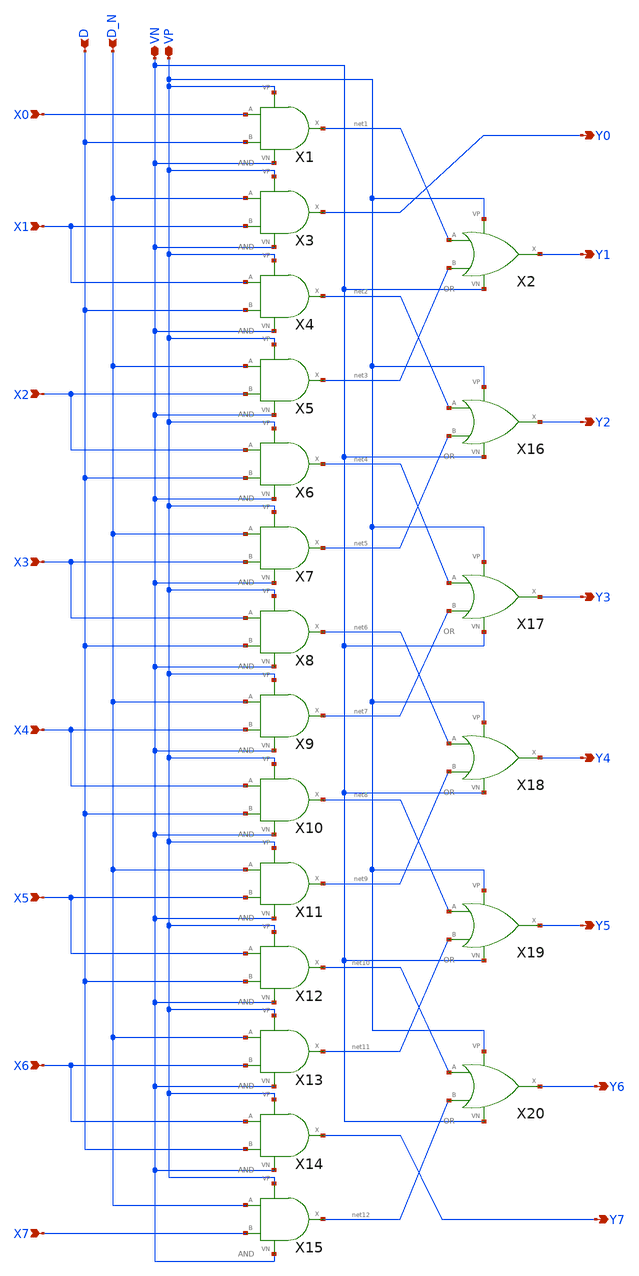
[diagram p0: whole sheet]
** sch_path: projekat_spice/layout/shifter/SHIFTER.sch
**.subckt SHIFTER VP VN X0 X1 X2 X3 X4 X5 X6 X7 D D_N Y0 Y1 Y2 Y3 Y4 Y5 Y6 Y7
*.iopin VP
*.iopin VN
*.ipin X0
*.ipin X1
*.ipin X2
*.ipin X3
*.ipin X4
*.ipin X5
*.ipin X6
*.ipin X7
*.ipin D
*.ipin D_N
*.opin Y0
*.opin Y1
*.opin Y2
*.opin Y3
*.opin Y4
*.opin Y5
*.opin Y6
*.opin Y7
X1 X0 D net1 VP VN AND
X3 D_N X1 Y0 VP VN AND
X4 X1 D net2 VP VN AND
X5 D_N X2 net3 VP VN AND
X6 X2 D net4 VP VN AND
X7 D_N X3 net5 VP VN AND
X8 X3 D net6 VP VN AND
X9 D_N X4 net7 VP VN AND
X10 X4 D net8 VP VN AND
X11 D_N X5 net9 VP VN AND
X12 X5 D net10 VP VN AND
X13 D_N X6 net11 VP VN AND
X14 X6 D Y7 VP VN AND
X15 D_N X7 net12 VP VN AND
X2 net1 net3 Y1 VP VN OR
X16 net2 net5 Y2 VP VN OR
X17 net4 net7 Y3 VP VN OR
X18 net6 net9 Y4 VP VN OR
X19 net8 net11 Y5 VP VN OR
X20 net10 net12 Y6 VP VN OR
**.ends

* expanding   symbol:  /home/mihailo/projekat_sky130/projekat_layout/and/AND.sym # of pins=5
** sym_path: projekat_spice/layout/and/AND.sym
** sch_path: projekat_spice/layout/and/AND.sch
.subckt AND A B X VP VN
*.ipin A
*.ipin B
*.iopin VN
*.iopin VP
*.opin X
XM1 net1 A net2 VN sky130_fd_pr__nfet_01v8 L=0.15 W=1 nf=1 ad='int((nf+1)/2) * W/nf * 0.29' as='int((nf+2)/2) * W/nf * 0.29'
+ pd='2*int((nf+1)/2) * (W/nf + 0.29)' ps='2*int((nf+2)/2) * (W/nf + 0.29)' nrd='0.29 / W' nrs='0.29 / W'
+ sa=0 sb=0 sd=0 mult=1 m=1
XM2 net1 A VP VP sky130_fd_pr__pfet_01v8 L=0.15 W=1 nf=1 ad='int((nf+1)/2) * W/nf * 0.29' as='int((nf+2)/2) * W/nf * 0.29'
+ pd='2*int((nf+1)/2) * (W/nf + 0.29)' ps='2*int((nf+2)/2) * (W/nf + 0.29)' nrd='0.29 / W' nrs='0.29 / W'
+ sa=0 sb=0 sd=0 mult=1 m=1
XM3 net1 B VP VP sky130_fd_pr__pfet_01v8 L=0.15 W=1 nf=1 ad='int((nf+1)/2) * W/nf * 0.29' as='int((nf+2)/2) * W/nf * 0.29'
+ pd='2*int((nf+1)/2) * (W/nf + 0.29)' ps='2*int((nf+2)/2) * (W/nf + 0.29)' nrd='0.29 / W' nrs='0.29 / W'
+ sa=0 sb=0 sd=0 mult=1 m=1
XM4 net2 B VN VN sky130_fd_pr__nfet_01v8 L=0.15 W=1 nf=1 ad='int((nf+1)/2) * W/nf * 0.29' as='int((nf+2)/2) * W/nf * 0.29'
+ pd='2*int((nf+1)/2) * (W/nf + 0.29)' ps='2*int((nf+2)/2) * (W/nf + 0.29)' nrd='0.29 / W' nrs='0.29 / W'
+ sa=0 sb=0 sd=0 mult=1 m=1
XM5 X net1 VN VN sky130_fd_pr__nfet_01v8 L=0.15 W=1 nf=1 ad='int((nf+1)/2) * W/nf * 0.29' as='int((nf+2)/2) * W/nf * 0.29'
+ pd='2*int((nf+1)/2) * (W/nf + 0.29)' ps='2*int((nf+2)/2) * (W/nf + 0.29)' nrd='0.29 / W' nrs='0.29 / W'
+ sa=0 sb=0 sd=0 mult=1 m=1
XM6 X net1 VP VP sky130_fd_pr__pfet_01v8 L=0.15 W=1 nf=1 ad='int((nf+1)/2) * W/nf * 0.29' as='int((nf+2)/2) * W/nf * 0.29'
+ pd='2*int((nf+1)/2) * (W/nf + 0.29)' ps='2*int((nf+2)/2) * (W/nf + 0.29)' nrd='0.29 / W' nrs='0.29 / W'
+ sa=0 sb=0 sd=0 mult=1 m=1
.ends


* expanding   symbol:  /home/mihailo/projekat_sky130/projekat_layout/or/OR.sym # of pins=5
** sym_path: projekat_spice/layout/or/OR.sym
** sch_path: projekat_spice/layout/or/OR.sch
.subckt OR A B X VP VN
*.opin X
*.ipin A
*.ipin B
*.iopin VP
*.iopin VN
XM1 net2 A VN VN sky130_fd_pr__nfet_01v8 L=0.15 W=1 nf=1 ad='int((nf+1)/2) * W/nf * 0.29' as='int((nf+2)/2) * W/nf * 0.29'
+ pd='2*int((nf+1)/2) * (W/nf + 0.29)' ps='2*int((nf+2)/2) * (W/nf + 0.29)' nrd='0.29 / W' nrs='0.29 / W'
+ sa=0 sb=0 sd=0 mult=1 m=1
XM2 net1 A VP VP sky130_fd_pr__pfet_01v8 L=0.15 W=1 nf=1 ad='int((nf+1)/2) * W/nf * 0.29' as='int((nf+2)/2) * W/nf * 0.29'
+ pd='2*int((nf+1)/2) * (W/nf + 0.29)' ps='2*int((nf+2)/2) * (W/nf + 0.29)' nrd='0.29 / W' nrs='0.29 / W'
+ sa=0 sb=0 sd=0 mult=1 m=1
XM3 net2 B net1 VP sky130_fd_pr__pfet_01v8 L=0.15 W=1 nf=1 ad='int((nf+1)/2) * W/nf * 0.29' as='int((nf+2)/2) * W/nf * 0.29'
+ pd='2*int((nf+1)/2) * (W/nf + 0.29)' ps='2*int((nf+2)/2) * (W/nf + 0.29)' nrd='0.29 / W' nrs='0.29 / W'
+ sa=0 sb=0 sd=0 mult=1 m=1
XM4 net2 B VN VN sky130_fd_pr__nfet_01v8 L=0.15 W=1 nf=1 ad='int((nf+1)/2) * W/nf * 0.29' as='int((nf+2)/2) * W/nf * 0.29'
+ pd='2*int((nf+1)/2) * (W/nf + 0.29)' ps='2*int((nf+2)/2) * (W/nf + 0.29)' nrd='0.29 / W' nrs='0.29 / W'
+ sa=0 sb=0 sd=0 mult=1 m=1
XM5 X net2 VN VN sky130_fd_pr__nfet_01v8 L=0.15 W=1 nf=1 ad='int((nf+1)/2) * W/nf * 0.29' as='int((nf+2)/2) * W/nf * 0.29'
+ pd='2*int((nf+1)/2) * (W/nf + 0.29)' ps='2*int((nf+2)/2) * (W/nf + 0.29)' nrd='0.29 / W' nrs='0.29 / W'
+ sa=0 sb=0 sd=0 mult=1 m=1
XM6 X net2 VP VP sky130_fd_pr__pfet_01v8 L=0.15 W=1 nf=1 ad='int((nf+1)/2) * W/nf * 0.29' as='int((nf+2)/2) * W/nf * 0.29'
+ pd='2*int((nf+1)/2) * (W/nf + 0.29)' ps='2*int((nf+2)/2) * (W/nf + 0.29)' nrd='0.29 / W' nrs='0.29 / W'
+ sa=0 sb=0 sd=0 mult=1 m=1
.ends

.end
